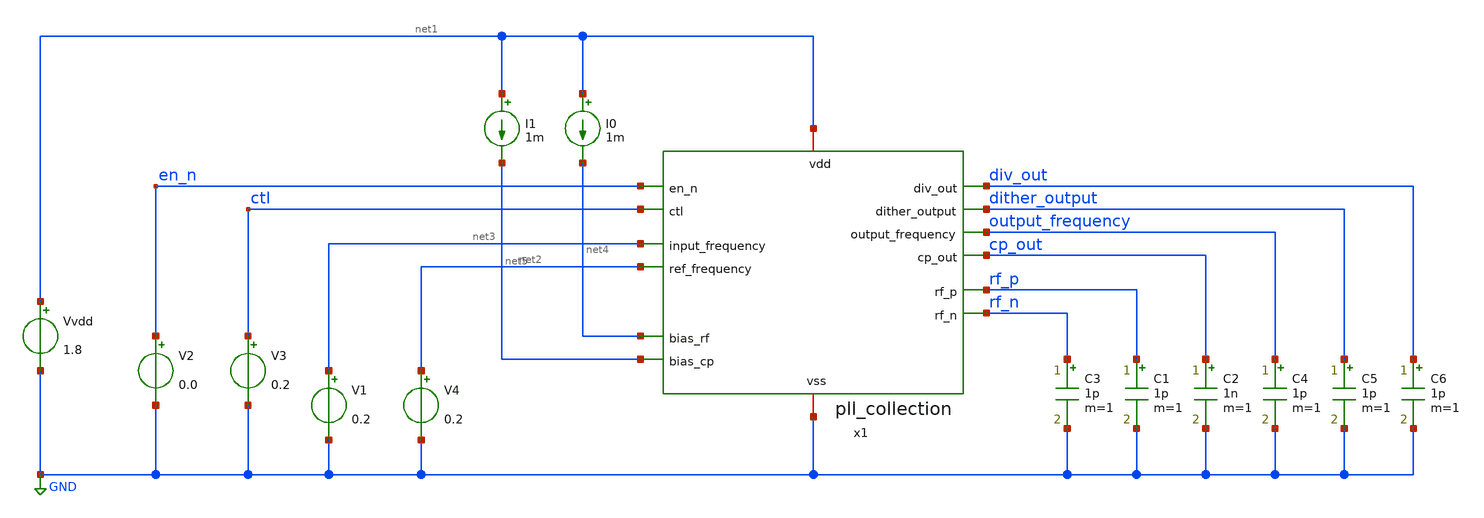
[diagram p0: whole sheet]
** sch_path: xschem/pll_collection/test/pll_collection_tb.sch
**.subckt pll_collection_tb
x1 net1 en_n ctl div_out GND dither_output output_frequency cp_out rf_p rf_n net3 net4 net5 net2
+ pll_collection
Vvdd net1 GND 1.8
V2 en_n GND 0.0
V3 ctl GND 0.2
C2 cp_out GND 1n m=1
V1 net3 GND 0.2
V4 net2 GND 0.2
I0 net1 net4 1m
I1 net1 net5 1m
C1 rf_p GND 1p m=1
C3 rf_n GND 1p m=1
C4 output_frequency GND 1p m=1
C5 dither_output GND 1p m=1
C6 div_out GND 1p m=1
**** begin user architecture code


.param temp=27
.temp 27

*.save v(ip) v(in) v(vctl) i(vdd)

.include sky130_fd_pr/cells/rf_nfet_01v8_lvt/sky130_fd_pr__rf_nfet_01v8_lvt_aM04W5p00L0p15.spice
.include sky130_fd_pr/cells/rf_nfet_01v8_lvt/sky130_fd_pr__rf_nfet_01v8_lvt_aM02W3p00L0p15.spice
.include sky130_fd_pr/cells/rf_nfet_01v8_lvt/sky130_fd_pr__rf_nfet_01v8_lvt_aM02W1p65L0p15.spice

.include sky130_fd_pr/cells/rf_pfet_01v8_lvt/sky130_fd_pr__rf_pfet_01v8_lvt_aM04W5p00L0p35.spice
.include sky130_fd_pr/cells/rf_pfet_01v8_lvt/sky130_fd_pr__rf_pfet_01v8_lvt_aM04W3p00L0p35.spice
.include sky130_fd_pr/cells/rf_pfet_01v8_lvt/sky130_fd_pr__rf_pfet_01v8_lvt_aM04W5p00L0p35.spice
.include sky130_fd_pr/cells/rf_pfet_01v8_lvt/sky130_fd_pr__rf_pfet_01v8_lvt_aM04W5p00L0p50.spice
.include sky130_fd_pr/cells/rf_pfet_01v8_lvt/sky130_fd_pr__rf_pfet_01v8_lvt_aM02W3p00L0p35.spice
.include sky130_fd_pr/cells/rf_pfet_01v8_lvt/sky130_fd_pr__rf_pfet_01v8_lvt_aM02W5p00L0p35.spice

.include sky130_fd_pr/cells/rf_pfet_01v8/sky130_fd_pr__rf_pfet_01v8_aM02W1p65L0p15.spice
.include sky130_fd_pr/cells/rf_pfet_01v8/sky130_fd_pr__rf_pfet_01v8_aM02W3p00L0p15.spice
.include sky130_fd_pr/cells/rf_pfet_01v8/sky130_fd_pr__rf_pfet_01v8_aM02W5p00L0p15.spice
.include sky130_fd_pr/cells/rf_pfet_01v8/sky130_fd_pr__rf_pfet_01v8_aM02W3p00L0p25.spice
.include sky130_fd_pr/cells/rf_pfet_01v8/sky130_fd_pr__rf_pfet_01v8_aM02W5p00L0p25.spice
.include sky130_fd_pr/cells/rf_pfet_01v8/sky130_fd_pr__rf_pfet_01v8_aF04W2p00L0p15.spice
.include sky130_fd_pr/cells/rf_pfet_01v8/sky130_fd_pr__rf_pfet_01v8_aF04W3p00L0p15.spice
.include sky130_fd_pr/cells/rf_pfet_01v8/sky130_fd_pr__rf_pfet_01v8_aM02W1p65L0p25.spice

.include sky130_fd_pr/cells/rf_nfet_01v8_lvt/sky130_fd_pr__rf_nfet_01v8_lvt_aF06W3p00L0p15.spice
.include sky130_fd_pr/cells/rf_nfet_01v8_lvt/sky130_fd_pr__rf_nfet_01v8_lvt_aF06W1p65L0p15.spice
.include sky130_fd_pr/cells/rf_nfet_01v8_lvt/sky130_fd_pr__rf_nfet_01v8_lvt_aF04W1p65L0p15.spice
.include sky130_fd_pr/cells/rf_nfet_01v8_lvt/sky130_fd_pr__rf_nfet_01v8_lvt_aF02W1p65L0p15.spice
.include sky130_fd_pr/cells/rf_nfet_01v8_lvt/sky130_fd_pr__rf_nfet_01v8_lvt_aF02W0p84L0p15.spice


.lib sky130_fd_pr/models/sky130.lib.spice tt
*.include sky130_fd_pr/models/corners/tt.spice


.tran 0.01n 1000n uic
.param vdd=1.8
.param vctl=0.2


**** end user architecture code
**.ends
.GLOBAL GND
**** begin user architecture code

**** end user architecture code
.end
